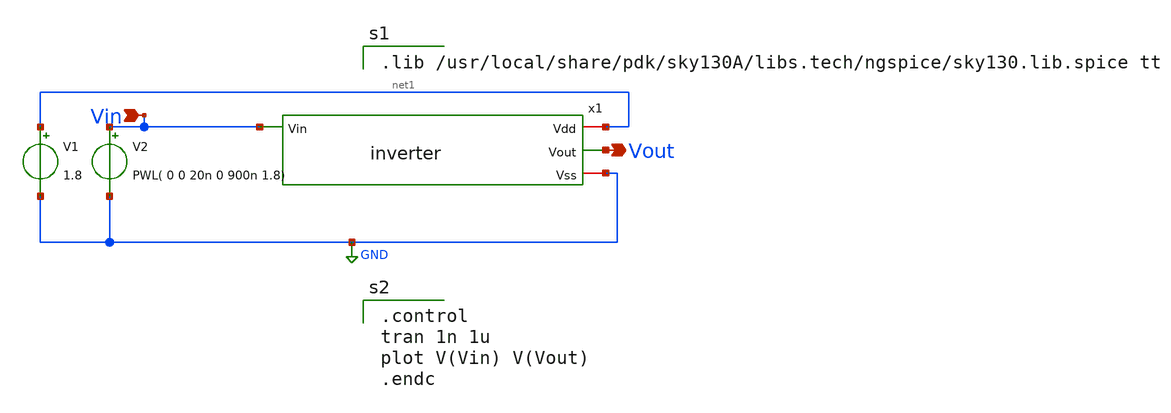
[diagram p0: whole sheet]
** sch_path: Lab1/inverter_tb.sch
**.subckt inverter_tb Vout Vin
*.opin Vout
*.ipin Vin
x1 net1 Vin Vout GND inverter
V1 net1 GND 1.8
V2 Vin GND PWL( 0 0 20n 0 900n 1.8)
**** begin user architecture code

.lib /usr/local/share/pdk/sky130A/libs.tech/ngspice/sky130.lib.spice tt


.control
tran 1n 1u
plot V(Vin) V(Vout)
.endc

**** end user architecture code
**.ends

* expanding   symbol:  inverter.sym # of pins=4
** sym_path: Lab1/inverter.sym
** sch_path: Lab1/inverter.sch
.subckt inverter Vdd Vin Vout Vss
*.ipin Vin
*.opin Vout
*.iopin Vdd
*.iopin Vss
XM1 Vout Vin Vss Vss sky130_fd_pr__nfet_01v8 L=0.18 W=4.5 nf=3 ad='int((3 + 1)/2) * 4.5 / 3 * 0.29' as='int((3 + 2)/2) * 4.5 / 3 * 0.29'
+ pd='2*int((3 + 1)/2) * (4.5 / 3 + 0.29)' ps='2*int((3 + 2)/2) * (4.5 / 3 + 0.29)' nrd='0.29 / 4.5 ' nrs='0.29 / 4.5 '
+ sa=0 sb=0 sd=0 mult=1 m=1
XM2 Vout Vin Vdd Vdd sky130_fd_pr__pfet_01v8 L=0.18 W=3 nf=3 ad='int((3 + 1)/2) * 3 / 3 * 0.29' as='int((3 + 2)/2) * 3 / 3 * 0.29'
+ pd='2*int((3 + 1)/2) * (3 / 3 + 0.29)' ps='2*int((3 + 2)/2) * (3 / 3 + 0.29)' nrd='0.29 / 3 ' nrs='0.29 / 3 '
+ sa=0 sb=0 sd=0 mult=1 m=1
.ends

.GLOBAL GND
.end
